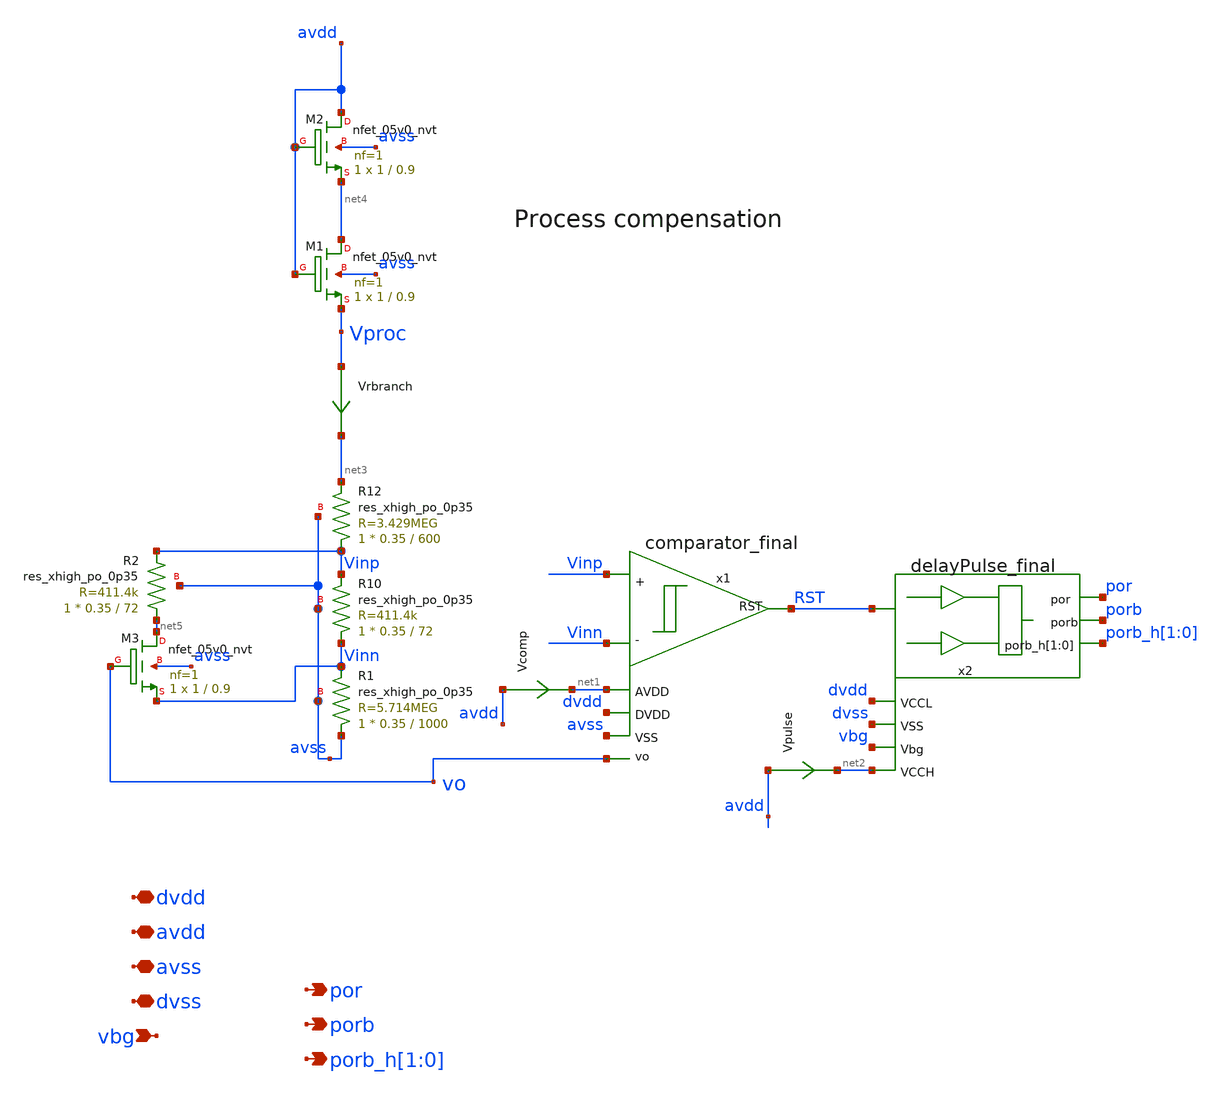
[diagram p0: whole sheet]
** sch_path: xschem/sky130_sw_ip__bgrref_por.sch
**.subckt sky130_sw_ip__bgrref_por avdd por avss dvdd porb vbg porb_h[1],porb_h[0] dvss
*.iopin avdd
*.opin por
*.iopin avss
*.iopin dvdd
*.opin porb
*.ipin vbg
*.opin porb_h[1],porb_h[0]
*.iopin dvss
x1 Vinn Vinp RST avss net1 dvdd vo comparator_final
XR1 avss Vinn avss sky130_fd_pr__res_xhigh_po_0p35 L=1000 mult=1 m=1
XR10 Vinn Vinp avss sky130_fd_pr__res_xhigh_po_0p35 L=72 mult=1 m=1
XR12 Vinp net3 avss sky130_fd_pr__res_xhigh_po_0p35 L=600 mult=1 m=1
x2 RST por dvdd dvss vbg net2 porb porb_h[1] porb_h[0] delayPulse_final
XM2 avdd avdd net4 avss sky130_fd_pr__nfet_05v0_nvt L=0.9 W=1 nf=1 ad='int((nf+1)/2) * W/nf * 0.29' as='int((nf+2)/2) * W/nf * 0.29'
+ pd='2*int((nf+1)/2) * (W/nf + 0.29)' ps='2*int((nf+2)/2) * (W/nf + 0.29)' nrd='0.29 / W' nrs='0.29 / W'
+ sa=0 sb=0 sd=0 mult=1 m=1
Vrbranch Vproc net3 0
.save i(vrbranch)
Vcomp avdd net1 0
.save i(vcomp)
Vpulse avdd net2 0
.save i(vpulse)
XM1 net4 avdd Vproc avss sky130_fd_pr__nfet_05v0_nvt L=0.9 W=1 nf=1 ad='int((nf+1)/2) * W/nf * 0.29'
+ as='int((nf+2)/2) * W/nf * 0.29' pd='2*int((nf+1)/2) * (W/nf + 0.29)' ps='2*int((nf+2)/2) * (W/nf + 0.29)'
+ nrd='0.29 / W' nrs='0.29 / W' sa=0 sb=0 sd=0 mult=1 m=1
XR2 net5 Vinp avss sky130_fd_pr__res_xhigh_po_0p35 L=72 mult=1 m=1
XM3 net5 vo Vinn avss sky130_fd_pr__nfet_05v0_nvt L=0.9 W=1 nf=1 ad='int((nf+1)/2) * W/nf * 0.29' as='int((nf+2)/2) * W/nf * 0.29'
+ pd='2*int((nf+1)/2) * (W/nf + 0.29)' ps='2*int((nf+2)/2) * (W/nf + 0.29)' nrd='0.29 / W' nrs='0.29 / W'
+ sa=0 sb=0 sd=0 mult=1 m=1
**.ends
.end
